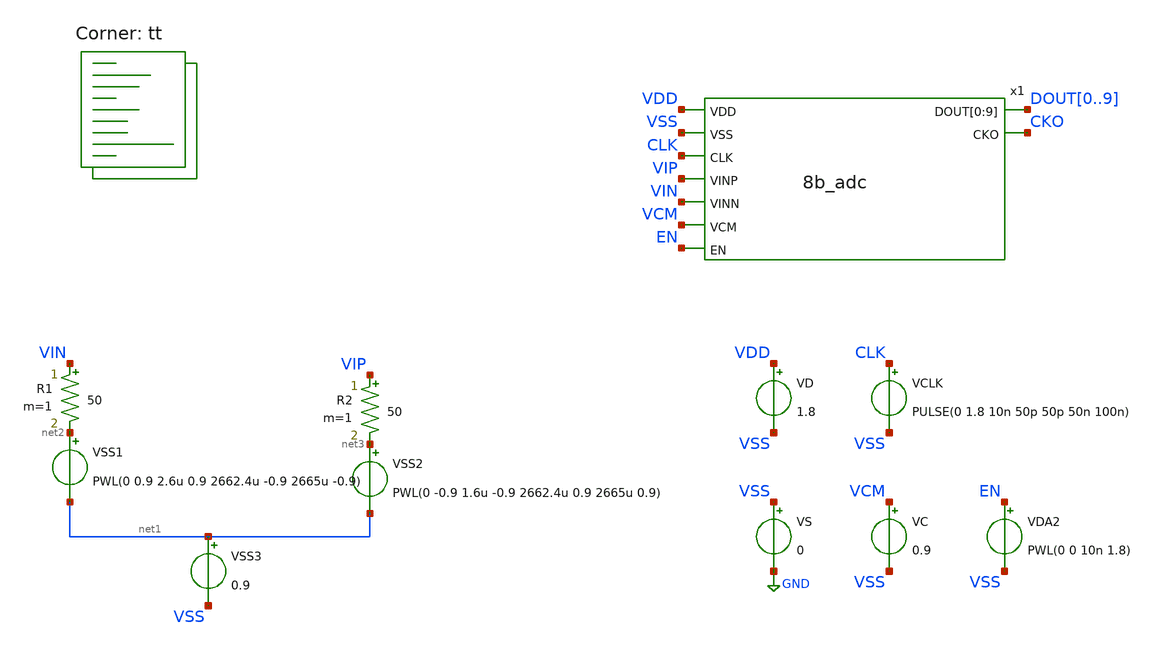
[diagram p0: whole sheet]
** sch_path: xschem/adc_tb_static.sch
**.subckt adc_tb_static
VS VSS GND 0
VD VDD VSS 1.8
VSS1 net2 net1 PWL(0 0.9 2.6u 0.9 2662.4u -0.9 2665u -0.9)
VSS2 net3 net1 PWL(0 -0.9 1.6u -0.9 2662.4u 0.9 2665u 0.9)
VSS3 net1 VSS 0.9
VCLK CLK VSS PULSE(0 1.8 10n 50p 50p 50n 100n)
R1 VIN net2 50 m=1
R2 VIP net3 50 m=1
x1 VDD VSS CLK VIP VIN VCM EN DOUT0 DOUT1 DOUT2 DOUT3 DOUT4 DOUT5 DOUT6 DOUT7 DOUT8 DOUT9 CKO 8b_adc
VC VCM VSS 0.9
VDA2 EN VSS PWL(0 0 10n 1.8)
**** begin user architecture code

** opencircuitdesign pdks install
* .lib $::SKYWATER_MODELS/sky130.lib.spice tt
.include $PDK_ROOT/$PDK/libs.ref/sky130_fd_sc_hd/spice/sky130_fd_sc_hd.spice



.option wnflag=0 bypass=1
.options method=gear reltol=1e-5 rawfile=binary
.options solver=klu nomod
.control
global netlist_dir .
set wr_singlescale
save x1.vcp x1.vcn vip vin clk vcm cko x1.cks x1.cksb vdd i(vd)  dout0 dout1 dout2 dout3 dout4 dout5
+ dout6 dout7 dout8 dout9
tran 100p 2.666m 0 100p uic ; Mengubah start time menjadi 10n
let pow = -i(vd)*vdd
meas tran inst_pow MAX pow from=10n to=2.666m
meas tran avg_pow  AVG pow from=10n to=2.666m
remzerovec
write adc10b_tb_static.raw
wrdata adc10b_tb_static.txt cko dout0 dout1 dout2 dout3 dout4 dout5 dout6 dout7 dout8 dout9 pow
quit 1
.endc


.lib $::SKYWATER_MODELS/sky130.lib.spice tt
**** end user architecture code
**.ends
.GLOBAL GND
.end
